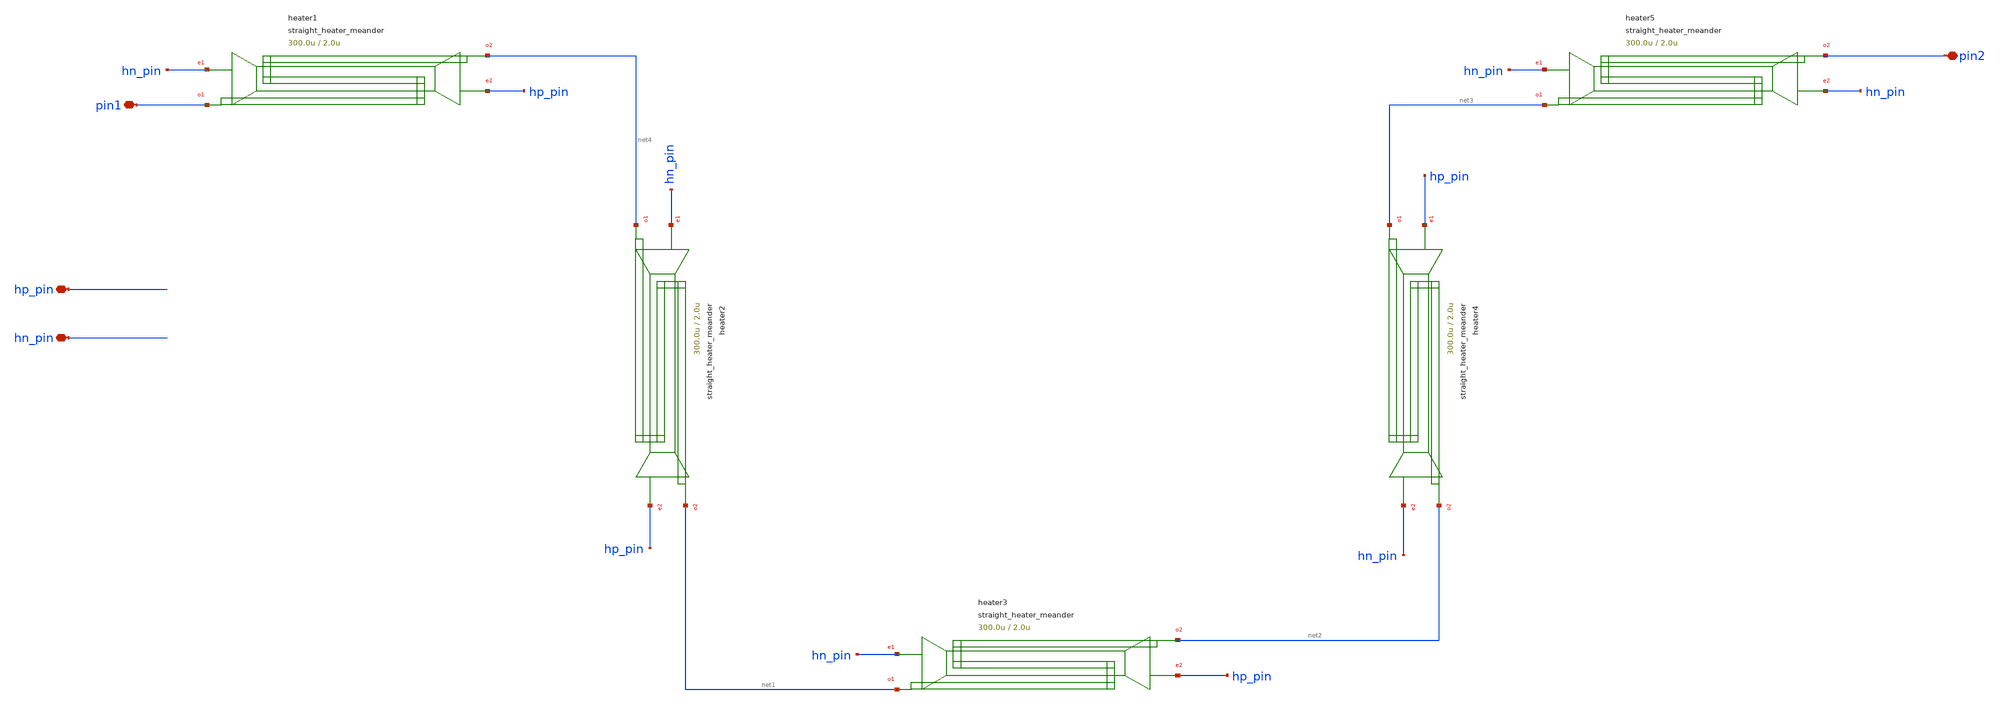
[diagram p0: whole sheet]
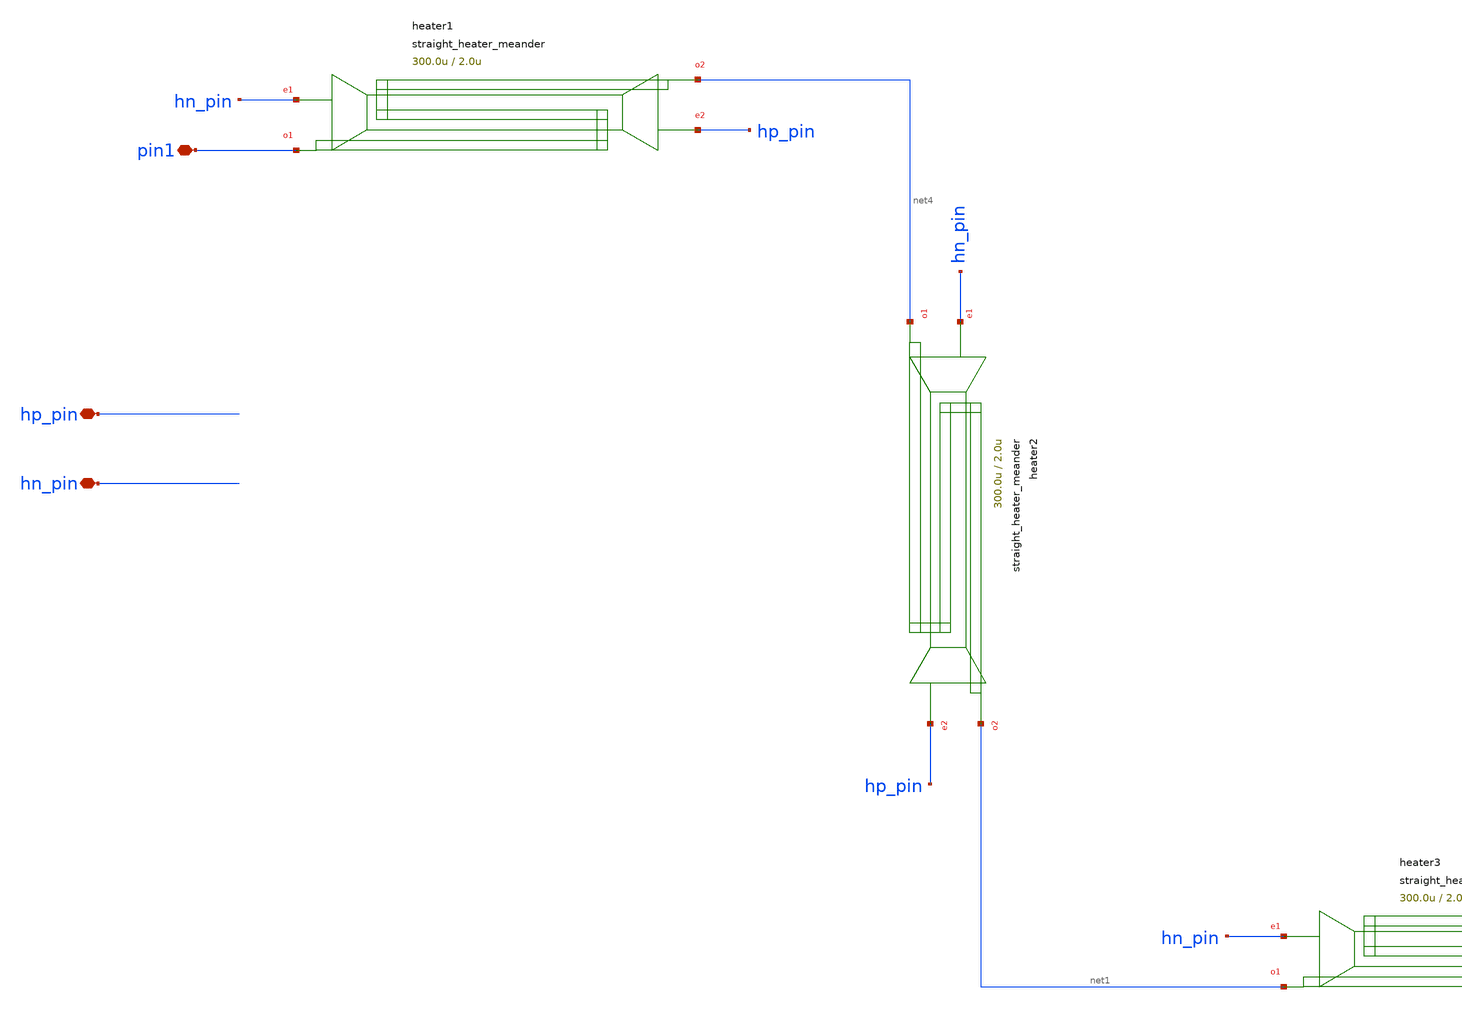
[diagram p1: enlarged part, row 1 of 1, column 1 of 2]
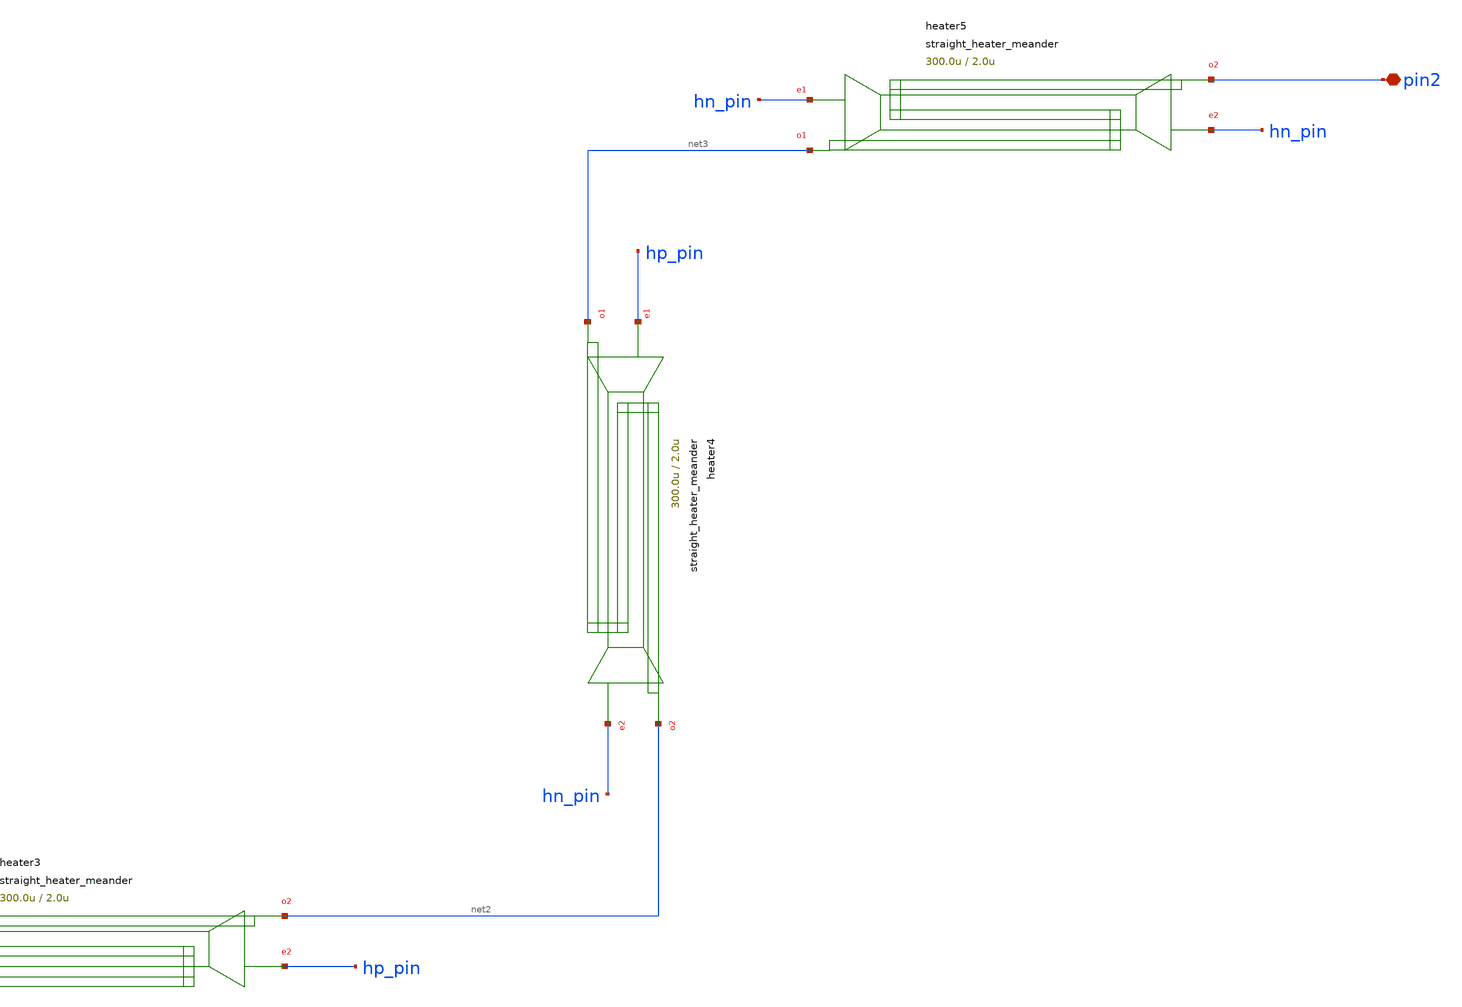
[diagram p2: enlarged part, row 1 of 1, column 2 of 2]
** sch_path: xschem/tests/test_sch/test_straight_heater_meander.sch
* Copyright (c) 2024, Mabrains LLC
* Licensed under the GNU Lesser General Public License, Version 3.0 (the "License");
* you may not use this file except in compliance with the License.
* GNU Lesser General Public License
* Version 3, 29 June 2007
* This program is free software: you can redistribute it and/or modify
* it under the terms of the GNU Lesser General Public License as published
* by the Free Software Foundation, either 3 of the License, or
* (at your option) any later version.
* This program is distributed in the hope that it will be useful,
* but WITHOUT ANY WARRANTY; without even the implied warranty of
* MERCHANTABILITY or FITNESS FOR A PARTICULAR PURPOSE.  See the
* GNU Lesser General Public License for more details.
* You should have received a copy of the GNU Lesser General Public License
* along with this program.  If not, see <https://www.gnu.org/licenses/>.
* SPDX-License-Identifier: LGPL-3.0
**.subckt test_straight_heater_meander hp_pin hn_pin pin1 pin2
*.iopin hp_pin
*.iopin hn_pin
*.iopin pin1
*.iopin pin2
Pheater1 pin1 net4 hn_pin hp_pin straight_heater_meander length=300.0u spacing=2.0u
+ heater_width=2.5u extension_length=15.0u radius=90u heater_taper_length=10.0u taper_length=10.0u
Pheater2 net4 net1 hn_pin hp_pin straight_heater_meander length=300.0u spacing=2.0u
+ heater_width=2.5u extension_length=15.0u radius=90u heater_taper_length=10.0u taper_length=10.0u
Pheater3 net1 net2 hn_pin hp_pin straight_heater_meander length=300.0u spacing=2.0u
+ heater_width=2.5u extension_length=15.0u radius=90u heater_taper_length=10.0u taper_length=10.0u
Pheater4 net3 net2 hp_pin hn_pin straight_heater_meander length=300.0u spacing=2.0u
+ heater_width=2.5u extension_length=15.0u radius=90u heater_taper_length=10.0u taper_length=10.0u
Pheater5 net3 pin2 hn_pin hn_pin straight_heater_meander length=300.0u spacing=2.0u
+ heater_width=2.5u extension_length=15.0u radius=90u heater_taper_length=10.0u taper_length=10.0u
**.ends
.end
